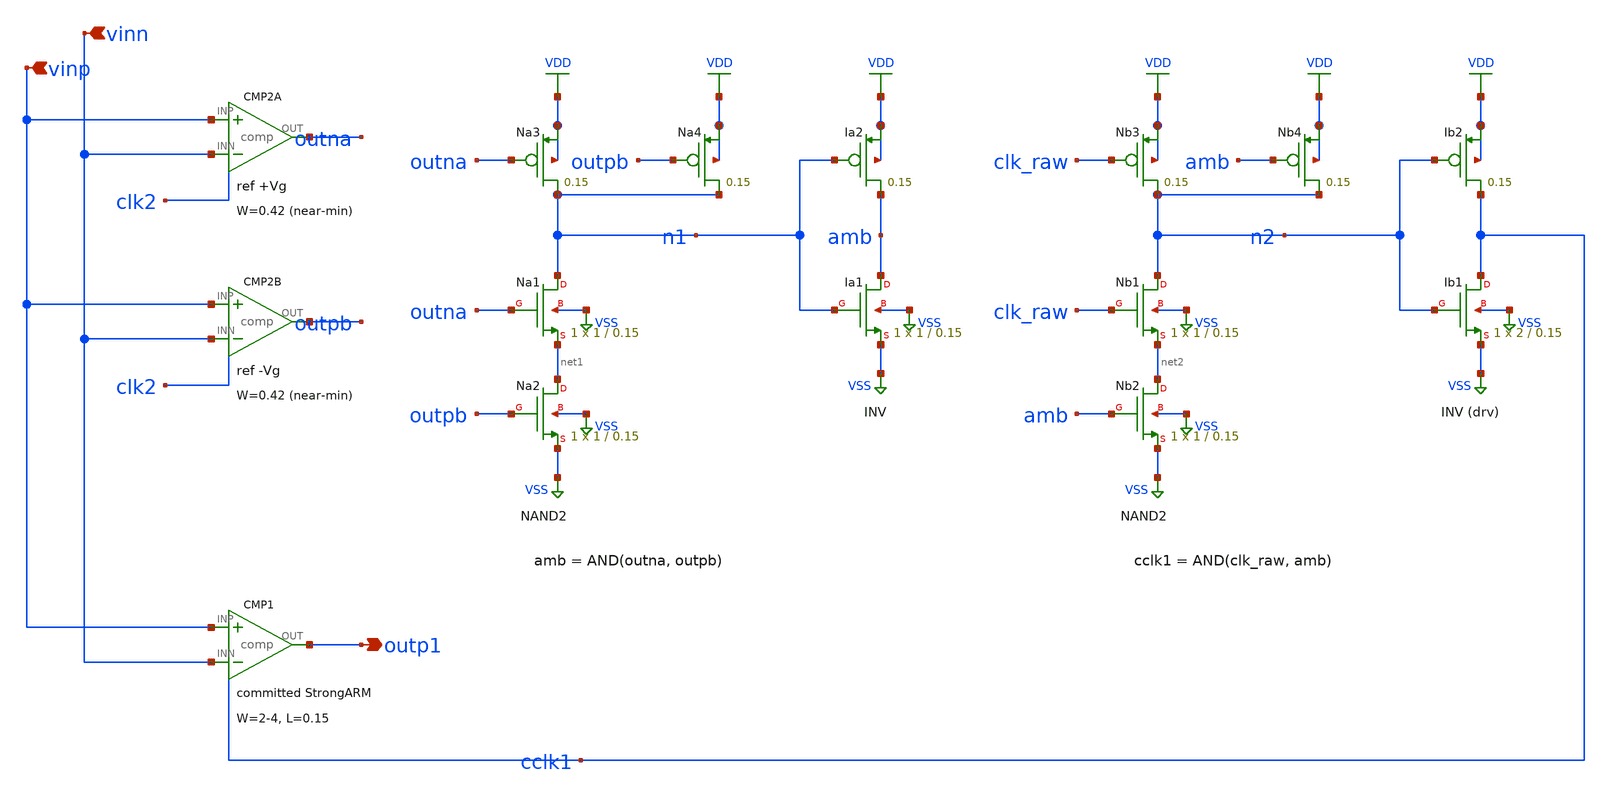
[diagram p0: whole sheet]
** sch_path: eda/hero/schematics/picoram_gating.sch
**.subckt picoram_gating vinp vinn outp1
*.ipin vinp
*.ipin vinn
*.opin outp1
XNa3 n1 outna VDD VDD sky130_fd_pr__sky130_fd_pr__pfet_01v8 L=0.15 W=1 nrd='0.29 / W' nrs='0.29 / W'
+ sa=0 sb=0 sd=0 mult=1 m=1
XNa4 n1 outpb VDD VDD sky130_fd_pr__sky130_fd_pr__pfet_01v8 L=0.15 W=1 nrd='0.29 / W' nrs='0.29 / W'
+ sa=0 sb=0 sd=0 mult=1 m=1
XNa1 n1 outna net1 VSS sky130_fd_pr__sky130_fd_pr__nfet_01v8 L=0.15 W=1 nrd='0.29 / W' nrs='0.29 / W'
+ sa=0 sb=0 sd=0 mult=1 m=1
XNa2 net1 outpb VSS VSS sky130_fd_pr__sky130_fd_pr__nfet_01v8 L=0.15 W=1 nrd='0.29 / W' nrs='0.29 / W'
+ sa=0 sb=0 sd=0 mult=1 m=1
XIa2 amb n1 VDD VDD sky130_fd_pr__sky130_fd_pr__pfet_01v8 L=0.15 W=2 nrd='0.29 / W' nrs='0.29 / W' sa=0
+ sb=0 sd=0 mult=1 m=1
XIa1 amb n1 VSS VSS sky130_fd_pr__sky130_fd_pr__nfet_01v8 L=0.15 W=1 nrd='0.29 / W' nrs='0.29 / W' sa=0
+ sb=0 sd=0 mult=1 m=1
XNb3 n2 clk_raw VDD VDD sky130_fd_pr__sky130_fd_pr__pfet_01v8 L=0.15 W=1 nrd='0.29 / W' nrs='0.29 / W'
+ sa=0 sb=0 sd=0 mult=1 m=1
XNb4 n2 amb VDD VDD sky130_fd_pr__sky130_fd_pr__pfet_01v8 L=0.15 W=1 nrd='0.29 / W' nrs='0.29 / W' sa=0
+ sb=0 sd=0 mult=1 m=1
XNb1 n2 clk_raw net2 VSS sky130_fd_pr__sky130_fd_pr__nfet_01v8 L=0.15 W=1 nrd='0.29 / W' nrs='0.29 / W'
+ sa=0 sb=0 sd=0 mult=1 m=1
XNb2 net2 amb VSS VSS sky130_fd_pr__sky130_fd_pr__nfet_01v8 L=0.15 W=1 nrd='0.29 / W' nrs='0.29 / W'
+ sa=0 sb=0 sd=0 mult=1 m=1
XIb2 cclk1 n2 VDD VDD sky130_fd_pr__sky130_fd_pr__pfet_01v8 L=0.15 W=4 nrd='0.29 / W' nrs='0.29 / W'
+ sa=0 sb=0 sd=0 mult=1 m=1
XIb1 cclk1 n2 VSS VSS sky130_fd_pr__sky130_fd_pr__nfet_01v8 L=0.15 W=2 nrd='0.29 / W' nrs='0.29 / W'
+ sa=0 sb=0 sd=0 mult=1 m=1
**.ends
.GLOBAL VDD
.GLOBAL VSS
.end
